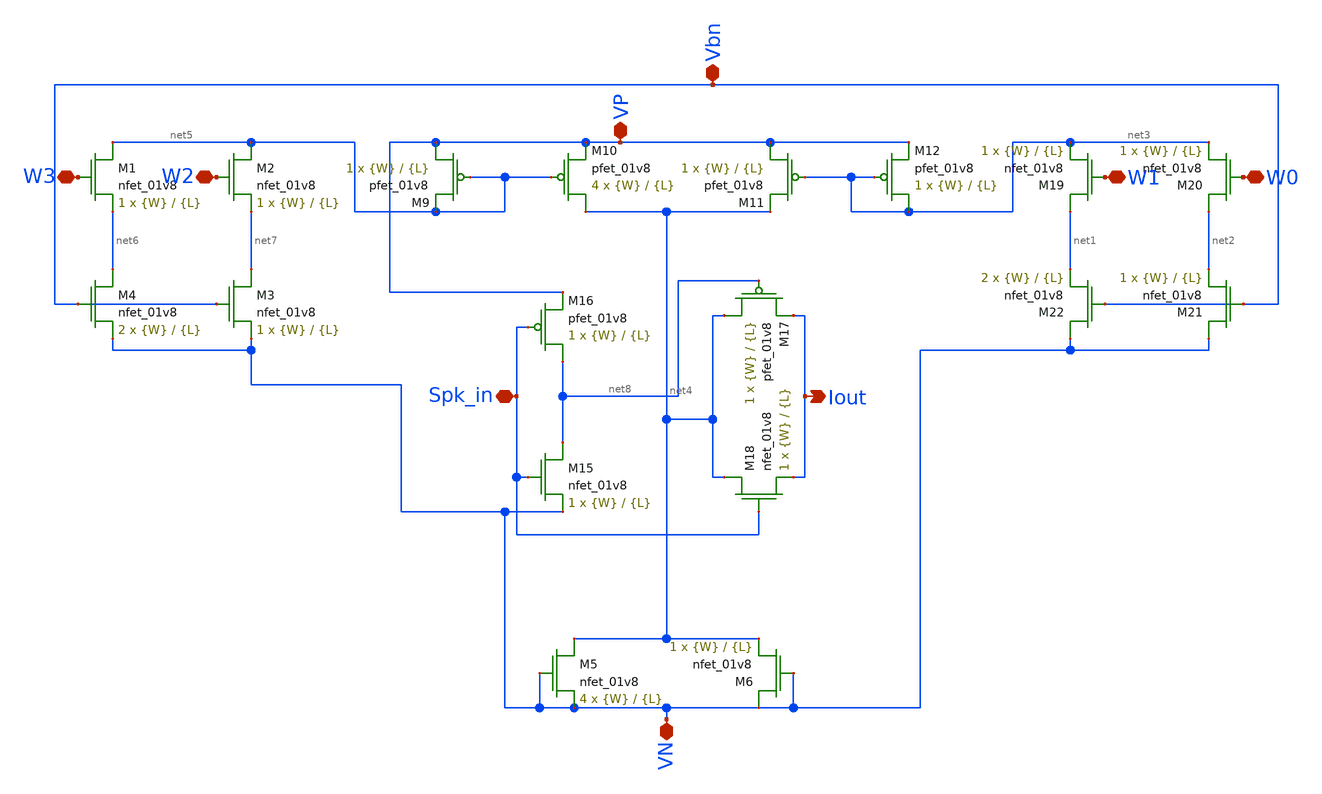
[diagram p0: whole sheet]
** sch_path: schematic/CMCI_synapse.sch
**.subckt CMCI_synapse Vbn VP Spk_in W3 W2 W1 W0 Iout VN
*.iopin Vbn
*.iopin VP
*.iopin Spk_in
*.iopin W3
*.iopin W2
*.iopin W1
*.iopin W0
*.opin Iout
*.iopin VN
XM1 net5 W3 net6 GND sky130_fd_pr__nfet_01v8 L={L} W={W} nf=1 ad='int((nf+1)/2) * W/nf * 0.29' as='int((nf+2)/2) * W/nf * 0.29'
+ pd='2*int((nf+1)/2) * (W/nf + 0.29)' ps='2*int((nf+2)/2) * (W/nf + 0.29)' nrd='0.29 / W' nrs='0.29 / W'
+ sa=0 sb=0 sd=0 mult=1 m=1
XM2 net5 W2 net7 GND sky130_fd_pr__nfet_01v8 L={L} W={W} nf=1 ad='int((nf+1)/2) * W/nf * 0.29' as='int((nf+2)/2) * W/nf * 0.29'
+ pd='2*int((nf+1)/2) * (W/nf + 0.29)' ps='2*int((nf+2)/2) * (W/nf + 0.29)' nrd='0.29 / W' nrs='0.29 / W'
+ sa=0 sb=0 sd=0 mult=1 m=1
XM3 net7 Vbn VN GND sky130_fd_pr__nfet_01v8 L={L} W={W} nf=1 ad='int((nf+1)/2) * W/nf * 0.29' as='int((nf+2)/2) * W/nf * 0.29'
+ pd='2*int((nf+1)/2) * (W/nf + 0.29)' ps='2*int((nf+2)/2) * (W/nf + 0.29)' nrd='0.29 / W' nrs='0.29 / W'
+ sa=0 sb=0 sd=0 mult=1 m=1
XM4 net6 Vbn VN GND sky130_fd_pr__nfet_01v8 L={L} W={W} nf=1 ad='int((nf+1)/2) * W/nf * 0.29' as='int((nf+2)/2) * W/nf * 0.29'
+ pd='2*int((nf+1)/2) * (W/nf + 0.29)' ps='2*int((nf+2)/2) * (W/nf + 0.29)' nrd='0.29 / W' nrs='0.29 / W'
+ sa=0 sb=0 sd=0 mult=2 m=2
XM9 VP net5 net5 VDD sky130_fd_pr__pfet_01v8 L={L} W={W} nf=1 ad='int((nf+1)/2) * W/nf * 0.29' as='int((nf+2)/2) * W/nf * 0.29'
+ pd='2*int((nf+1)/2) * (W/nf + 0.29)' ps='2*int((nf+2)/2) * (W/nf + 0.29)' nrd='0.29 / W' nrs='0.29 / W'
+ sa=0 sb=0 sd=0 mult=1 m=1
XM10 net4 net5 VP VDD sky130_fd_pr__pfet_01v8 L={L} W={W} nf=1 ad='int((nf+1)/2) * W/nf * 0.29' as='int((nf+2)/2) * W/nf * 0.29'
+ pd='2*int((nf+1)/2) * (W/nf + 0.29)' ps='2*int((nf+2)/2) * (W/nf + 0.29)' nrd='0.29 / W' nrs='0.29 / W'
+ sa=0 sb=0 sd=0 mult=4 m=4
XM11 VP net3 net4 VDD sky130_fd_pr__pfet_01v8 L={L} W={W} nf=1 ad='int((nf+1)/2) * W/nf * 0.29' as='int((nf+2)/2) * W/nf * 0.29'
+ pd='2*int((nf+1)/2) * (W/nf + 0.29)' ps='2*int((nf+2)/2) * (W/nf + 0.29)' nrd='0.29 / W' nrs='0.29 / W'
+ sa=0 sb=0 sd=0 mult=1 m=1
XM12 net3 net3 VP VDD sky130_fd_pr__pfet_01v8 L={L} W={W} nf=1 ad='int((nf+1)/2) * W/nf * 0.29' as='int((nf+2)/2) * W/nf * 0.29'
+ pd='2*int((nf+1)/2) * (W/nf + 0.29)' ps='2*int((nf+2)/2) * (W/nf + 0.29)' nrd='0.29 / W' nrs='0.29 / W'
+ sa=0 sb=0 sd=0 mult=1 m=1
XM15 net8 Spk_in VN GND sky130_fd_pr__nfet_01v8 L={L} W={W} nf=1 ad='int((nf+1)/2) * W/nf * 0.29' as='int((nf+2)/2) * W/nf * 0.29'
+ pd='2*int((nf+1)/2) * (W/nf + 0.29)' ps='2*int((nf+2)/2) * (W/nf + 0.29)' nrd='0.29 / W' nrs='0.29 / W'
+ sa=0 sb=0 sd=0 mult=1 m=1
XM16 net8 Spk_in VP VDD sky130_fd_pr__pfet_01v8 L={L} W={W} nf=1 ad='int((nf+1)/2) * W/nf * 0.29' as='int((nf+2)/2) * W/nf * 0.29'
+ pd='2*int((nf+1)/2) * (W/nf + 0.29)' ps='2*int((nf+2)/2) * (W/nf + 0.29)' nrd='0.29 / W' nrs='0.29 / W'
+ sa=0 sb=0 sd=0 mult=1 m=1
XM17 net4 net8 Iout VDD sky130_fd_pr__pfet_01v8 L={L} W={W} nf=1 ad='int((nf+1)/2) * W/nf * 0.29' as='int((nf+2)/2) * W/nf * 0.29'
+ pd='2*int((nf+1)/2) * (W/nf + 0.29)' ps='2*int((nf+2)/2) * (W/nf + 0.29)' nrd='0.29 / W' nrs='0.29 / W'
+ sa=0 sb=0 sd=0 mult=1 m=1
XM18 net4 Spk_in Iout GND sky130_fd_pr__nfet_01v8 L={L} W={W} nf=1 ad='int((nf+1)/2) * W/nf * 0.29' as='int((nf+2)/2) * W/nf * 0.29'
+ pd='2*int((nf+1)/2) * (W/nf + 0.29)' ps='2*int((nf+2)/2) * (W/nf + 0.29)' nrd='0.29 / W' nrs='0.29 / W'
+ sa=0 sb=0 sd=0 mult=1 m=1
XM19 net1 W1 net3 GND sky130_fd_pr__nfet_01v8 L={L} W={W} nf=1 ad='int((nf+1)/2) * W/nf * 0.29' as='int((nf+2)/2) * W/nf * 0.29'
+ pd='2*int((nf+1)/2) * (W/nf + 0.29)' ps='2*int((nf+2)/2) * (W/nf + 0.29)' nrd='0.29 / W' nrs='0.29 / W'
+ sa=0 sb=0 sd=0 mult=1 m=1
XM20 net2 W0 net3 GND sky130_fd_pr__nfet_01v8 L={L} W={W} nf=1 ad='int((nf+1)/2) * W/nf * 0.29' as='int((nf+2)/2) * W/nf * 0.29'
+ pd='2*int((nf+1)/2) * (W/nf + 0.29)' ps='2*int((nf+2)/2) * (W/nf + 0.29)' nrd='0.29 / W' nrs='0.29 / W'
+ sa=0 sb=0 sd=0 mult=1 m=1
XM21 VN Vbn net2 GND sky130_fd_pr__nfet_01v8 L={L} W={W} nf=1 ad='int((nf+1)/2) * W/nf * 0.29' as='int((nf+2)/2) * W/nf * 0.29'
+ pd='2*int((nf+1)/2) * (W/nf + 0.29)' ps='2*int((nf+2)/2) * (W/nf + 0.29)' nrd='0.29 / W' nrs='0.29 / W'
+ sa=0 sb=0 sd=0 mult=1 m=1
XM22 VN Vbn net1 GND sky130_fd_pr__nfet_01v8 L={L} W={W} nf=1 ad='int((nf+1)/2) * W/nf * 0.29' as='int((nf+2)/2) * W/nf * 0.29'
+ pd='2*int((nf+1)/2) * (W/nf + 0.29)' ps='2*int((nf+2)/2) * (W/nf + 0.29)' nrd='0.29 / W' nrs='0.29 / W'
+ sa=0 sb=0 sd=0 mult=2 m=2
XM5 net4 VN VN GND sky130_fd_pr__nfet_01v8 L={L} W={W} nf=1 ad='int((nf+1)/2) * W/nf * 0.29' as='int((nf+2)/2) * W/nf * 0.29'
+ pd='2*int((nf+1)/2) * (W/nf + 0.29)' ps='2*int((nf+2)/2) * (W/nf + 0.29)' nrd='0.29 / W' nrs='0.29 / W'
+ sa=0 sb=0 sd=0 mult=4 m=4
XM6 VN VN net4 GND sky130_fd_pr__nfet_01v8 L={L} W={W} nf=1 ad='int((nf+1)/2) * W/nf * 0.29' as='int((nf+2)/2) * W/nf * 0.29'
+ pd='2*int((nf+1)/2) * (W/nf + 0.29)' ps='2*int((nf+2)/2) * (W/nf + 0.29)' nrd='0.29 / W' nrs='0.29 / W'
+ sa=0 sb=0 sd=0 mult=1 m=1
**.ends
.end
